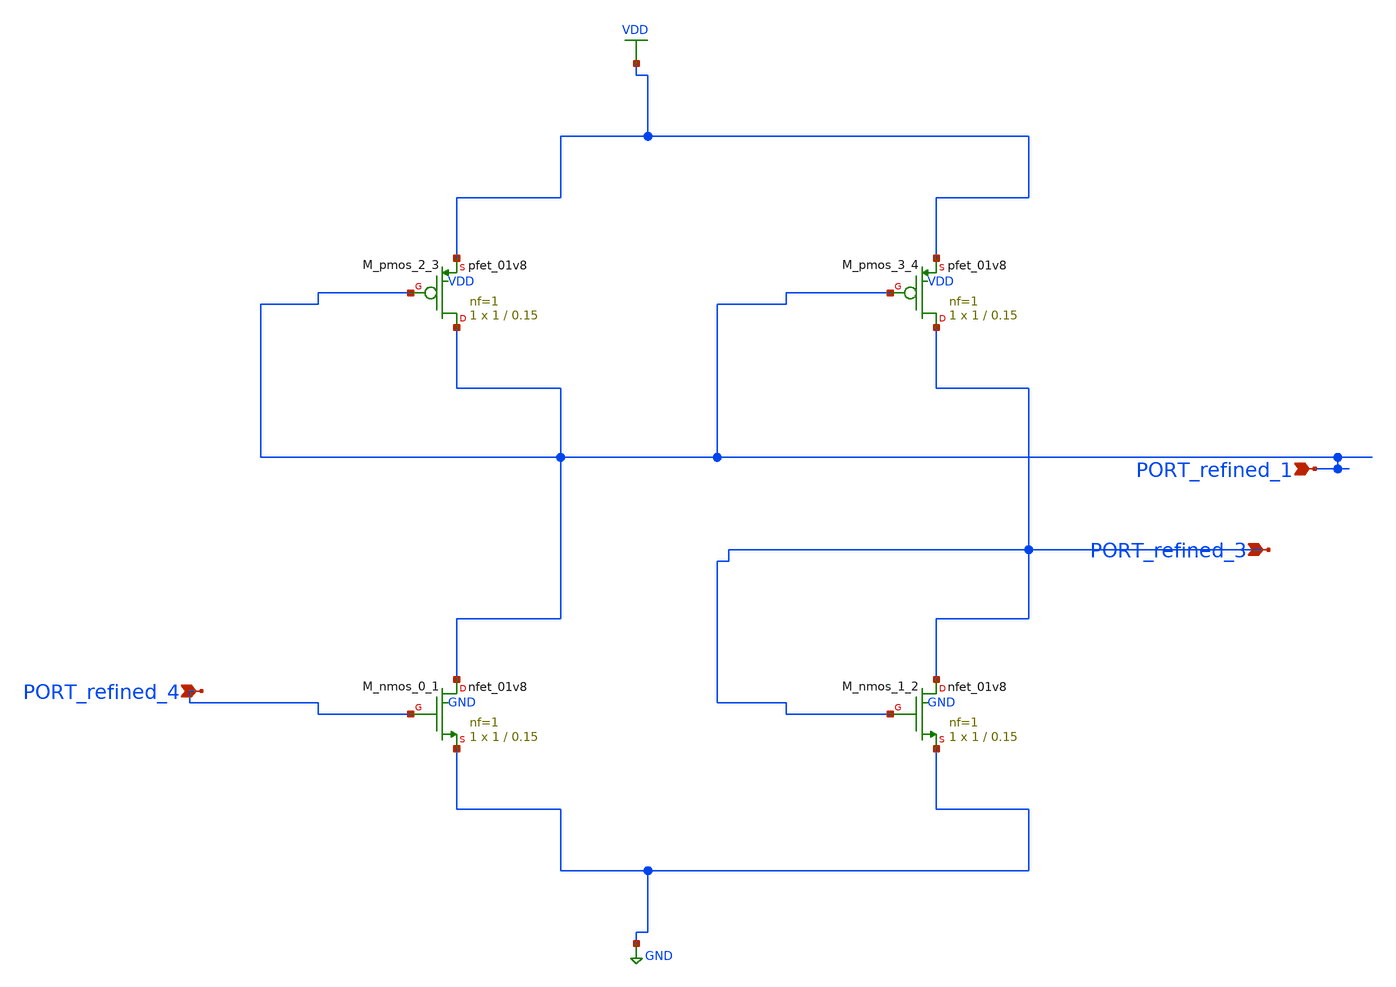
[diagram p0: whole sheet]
** sch_path: schematics/10_1109_ACCESS_2021_3050170_04_002.sch
**.subckt 10_1109_ACCESS_2021_3050170_04_002 PORT_refined_3 PORT_refined_4 PORT_refined_1
*.ipin PORT_refined_3
*.ipin PORT_refined_4
*.ipin PORT_refined_1
XM_nmos_0_1 PORT_refined_1 PORT_refined_4 GND GND sky130_fd_pr__nfet_01v8 L=0.15 W=1 nf=1 ad='int((1 + 1)/2) * 1 / 1 * 0.29'
+ as='int((1 + 2)/2) * 1 / 1 * 0.29' pd='2*int((1 + 1)/2) * (1 / 1 + 0.29)' ps='2*int((1 + 2)/2) * (1 / 1 + 0.29)'
+ nrd='0.29 / 1 ' nrs='0.29 / 1 ' sa=0 sb=0 sd=0 mult=1 m=1
XM_nmos_1_2 PORT_refined_3 PORT_refined_3 GND GND sky130_fd_pr__nfet_01v8 L=0.15 W=1 nf=1 ad='int((1 + 1)/2) * 1 / 1 * 0.29'
+ as='int((1 + 2)/2) * 1 / 1 * 0.29' pd='2*int((1 + 1)/2) * (1 / 1 + 0.29)' ps='2*int((1 + 2)/2) * (1 / 1 + 0.29)'
+ nrd='0.29 / 1 ' nrs='0.29 / 1 ' sa=0 sb=0 sd=0 mult=1 m=1
XM_pmos_2_3 PORT_refined_1 PORT_refined_1 VDD VDD sky130_fd_pr__pfet_01v8 L=0.15 W=1 nf=1 ad='int((1 + 1)/2) * 1 / 1 * 0.29'
+ as='int((1 + 2)/2) * 1 / 1 * 0.29' pd='2*int((1 + 1)/2) * (1 / 1 + 0.29)' ps='2*int((1 + 2)/2) * (1 / 1 + 0.29)'
+ nrd='0.29 / 1 ' nrs='0.29 / 1 ' sa=0 sb=0 sd=0 mult=1 m=1
XM_pmos_3_4 PORT_refined_3 PORT_refined_1 VDD VDD sky130_fd_pr__pfet_01v8 L=0.15 W=1 nf=1 ad='int((1 + 1)/2) * 1 / 1 * 0.29'
+ as='int((1 + 2)/2) * 1 / 1 * 0.29' pd='2*int((1 + 1)/2) * (1 / 1 + 0.29)' ps='2*int((1 + 2)/2) * (1 / 1 + 0.29)'
+ nrd='0.29 / 1 ' nrs='0.29 / 1 ' sa=0 sb=0 sd=0 mult=1 m=1
**.ends
.GLOBAL GND
.GLOBAL VDD
.end
